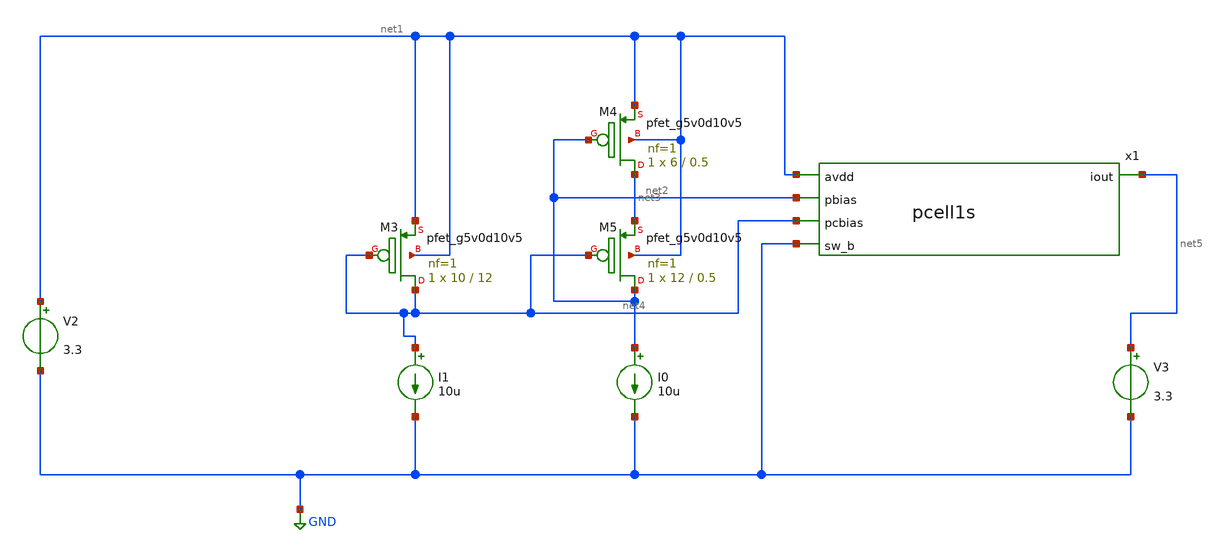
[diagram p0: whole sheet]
** sch_path: xschem/currentmirrorPtest_tb.sch
**.subckt currentmirrorPtest_tb
I0 net2 GND 10u
V2 net1 GND 3.3
V3 net5 GND 3.3
I1 net4 GND 10u
XM3 net4 net4 net1 net1 sky130_fd_pr__pfet_g5v0d10v5 L=12 W=10 nf=1 ad='int((nf+1)/2) * W/nf * 0.29'
+ as='int((nf+2)/2) * W/nf * 0.29' pd='2*int((nf+1)/2) * (W/nf + 0.29)' ps='2*int((nf+2)/2) * (W/nf + 0.29)'
+ nrd='0.29 / W' nrs='0.29 / W' sa=0 sb=0 sd=0 mult=1 m=1
XM4 net3 net2 net1 net1 sky130_fd_pr__pfet_g5v0d10v5 L=0.5 W=6 nf=1 ad='int((nf+1)/2) * W/nf * 0.29'
+ as='int((nf+2)/2) * W/nf * 0.29' pd='2*int((nf+1)/2) * (W/nf + 0.29)' ps='2*int((nf+2)/2) * (W/nf + 0.29)'
+ nrd='0.29 / W' nrs='0.29 / W' sa=0 sb=0 sd=0 mult=1 m=1
XM5 net2 net4 net3 net1 sky130_fd_pr__pfet_g5v0d10v5 L=0.5 W=12 nf=1 ad='int((nf+1)/2) * W/nf * 0.29'
+ as='int((nf+2)/2) * W/nf * 0.29' pd='2*int((nf+1)/2) * (W/nf + 0.29)' ps='2*int((nf+2)/2) * (W/nf + 0.29)'
+ nrd='0.29 / W' nrs='0.29 / W' sa=0 sb=0 sd=0 mult=1 m=1
x1 net1 net2 net4 GND net5 pcell1s
**** begin user architecture code
 .lib $::SKYWATER_MODELS/sky130.lib.spice tt

.param mc_mm_switch=0
.param mc_pr_switch=1



.option wnflag=0
.option savecurrents
.control
save all
dc v3 0 3.3 0.01
plot i(V3)
write currentmirrortb.raw
op
.endc


**** end user architecture code
**.ends

* expanding   symbol:  pcell1s.sym # of pins=5
** sym_path: xschem/pcell1s.sym
** sch_path: xschem/pcell1s.sch
.subckt pcell1s avdd pbias pcbias sw_b iout
*.ipin pbias
*.ipin pcbias
*.ipin sw_b
*.ipin avdd
*.opin iout
XM1 net1 pbias avdd avdd sky130_fd_pr__pfet_g5v0d10v5 L=0.5 W=6 nf=1 ad='int((nf+1)/2) * W/nf * 0.29'
+ as='int((nf+2)/2) * W/nf * 0.29' pd='2*int((nf+1)/2) * (W/nf + 0.29)' ps='2*int((nf+2)/2) * (W/nf + 0.29)'
+ nrd='0.29 / W' nrs='0.29 / W' sa=0 sb=0 sd=0 mult=1 m=1
XM2 net2 pcbias net1 avdd sky130_fd_pr__pfet_g5v0d10v5 L=0.5 W=12 nf=1 ad='int((nf+1)/2) * W/nf * 0.29'
+ as='int((nf+2)/2) * W/nf * 0.29' pd='2*int((nf+1)/2) * (W/nf + 0.29)' ps='2*int((nf+2)/2) * (W/nf + 0.29)'
+ nrd='0.29 / W' nrs='0.29 / W' sa=0 sb=0 sd=0 mult=1 m=1
XM3 iout sw_b net2 avdd sky130_fd_pr__pfet_g5v0d10v5 L=0.5 W=4 nf=1 ad='int((nf+1)/2) * W/nf * 0.29'
+ as='int((nf+2)/2) * W/nf * 0.29' pd='2*int((nf+1)/2) * (W/nf + 0.29)' ps='2*int((nf+2)/2) * (W/nf + 0.29)'
+ nrd='0.29 / W' nrs='0.29 / W' sa=0 sb=0 sd=0 mult=1 m=1
.ends

.GLOBAL GND
.end
